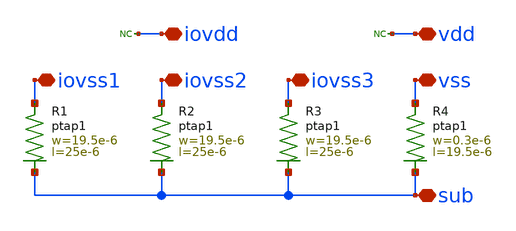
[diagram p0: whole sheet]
** sch_path: MSPHY6034-main/schematic/xschem/openpdk-libraries/ihp-sg13g2/sg13g2_io/xschem/sg13g2_Filler4000.sch
**.subckt sg13g2_Filler4000 iovss1 iovss2 iovss3 vss iovdd vdd sub
*.iopin iovss1
*.iopin iovss2
*.iopin iovss3
*.iopin vss
*.iopin iovdd
*.iopin vdd
*.iopin sub
XR3 iovss3 sub ptap1 R=1.7 w=19.5e-6 l=25e-6
XR4 vss sub ptap1 R=21.56 w=0.3e-6 l=19.5e-6
* noconn iovdd
* noconn vdd
XR1 iovss1 sub ptap1 R=1.7 w=19.5e-6 l=25e-6
XR2 iovss2 sub ptap1 R=1.7 w=19.5e-6 l=25e-6
**.ends
.end
